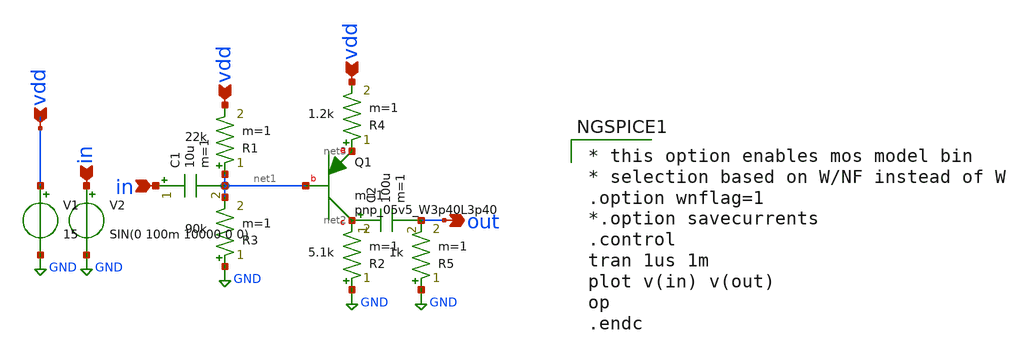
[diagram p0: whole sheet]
** sch_path: xschem/PNPam.sch
**.subckt PNPam vdd vdd vdd in in out
*.ipin vdd
*.ipin vdd
*.ipin vdd
*.ipin in
*.ipin in
*.opin out
XQ1 net2 net1 net3 sky130_fd_pr__pnp_05v5_W3p40L3p40 m=1
R1 net1 vdd 22k m=1
R2 GND net2 5.1k m=1
R3 GND net1 90k m=1
R4 net3 vdd 1.2k m=1
C1 in net1 10u m=1
V1 vdd GND 15
C2 net2 out 100u m=1
V2 in GND SIN(0 100m 10000 0 0)
R5 GND out 1k m=1
**** begin user architecture code

** opencircuitdesign pdks install
.lib $::SKYWATER_MODELS/sky130.lib.spice tt



* this option enables mos model bin
* selection based on W/NF instead of W
.option wnflag=1
*.option savecurrents
.control
tran 1us 1m
plot v(in) v(out)
op
.endc


**** end user architecture code
**.ends
.GLOBAL GND
.end
